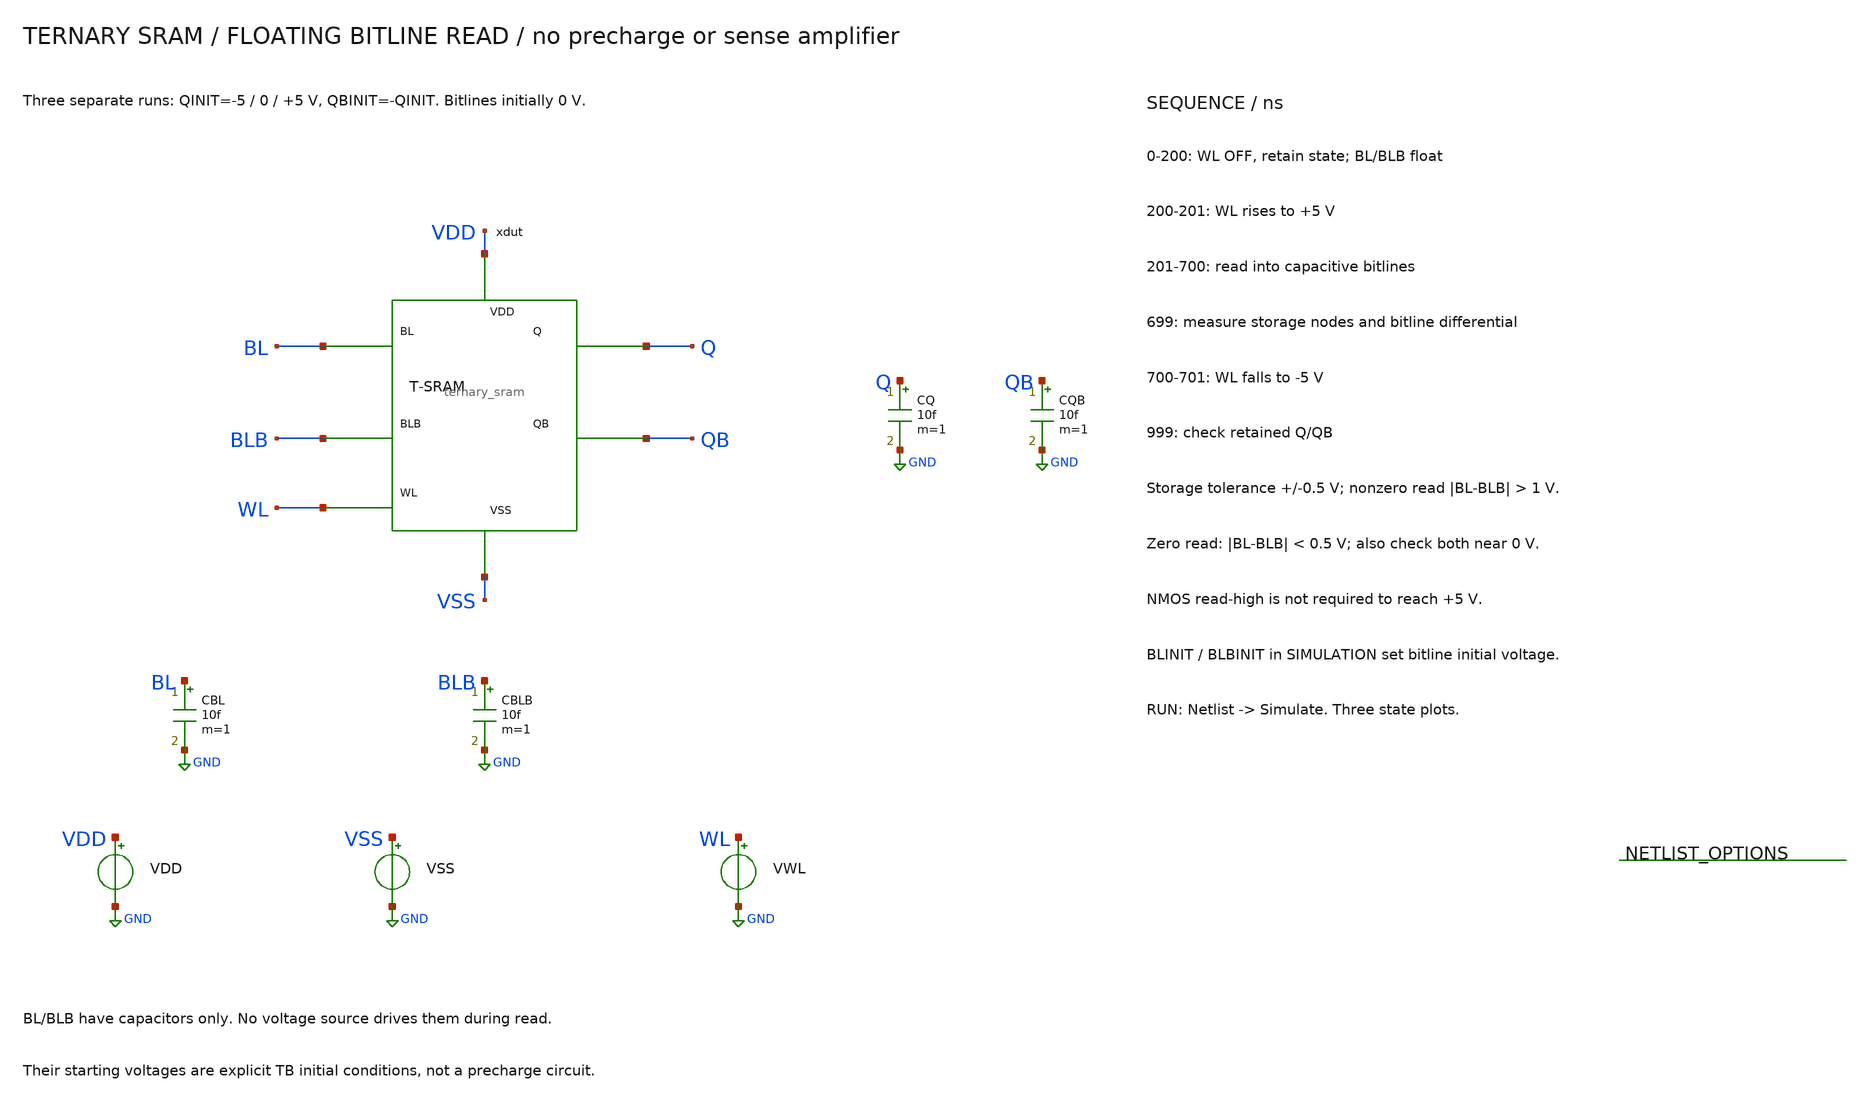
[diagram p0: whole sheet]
** sch_path: member_project/balanced-ternary-logic/PenguinEino/ternary_sram_read_tb.sch
**.subckt ternary_sram_read_tb
xdut BL BLB WL Q QB VDD VSS ternary_sram
CQ Q GND 10f m=1
CQB QB GND 10f m=1
CBL BL GND 10f m=1
CBLB BLB GND 10f m=1
VDD VDD GND 5
VSS VSS GND -5
VWL WL GND PWL(0 -5 200n -5 201n 5 700n 5 701n -5 1000n -5)
**** begin user architecture code
 .include $::LIB/ip62_models

.temp 27
.param QINIT=-5 BLINIT=0 BLBINIT=0
.ic v(Q)='QINIT' v(QB)='-QINIT' v(BL)='BLINIT' v(BLB)='BLBINIT'
.control
save all
set wr_singlescale
set wr_vecnames
setplot const
let failures=0
tran 0.2n 1000n 0 0.5n
let diff=v(BL)-v(BLB)
meas tran q0_199 find v(Q) at=199n
if abs(q0_199-(-5)) > 0.5
let const.failures=const.failures+1
echo FAIL: q0_199 expected -5 V
end
meas tran qb0_199 find v(QB) at=199n
if abs(qb0_199-(5)) > 0.5
let const.failures=const.failures+1
echo FAIL: qb0_199 expected 5 V
end
meas tran q0_699 find v(Q) at=699n
if abs(q0_699-(-5)) > 0.5
let const.failures=const.failures+1
echo FAIL: q0_699 expected -5 V
end
meas tran qb0_699 find v(QB) at=699n
if abs(qb0_699-(5)) > 0.5
let const.failures=const.failures+1
echo FAIL: qb0_699 expected 5 V
end
meas tran q0_999 find v(Q) at=999n
if abs(q0_999-(-5)) > 0.5
let const.failures=const.failures+1
echo FAIL: q0_999 expected -5 V
end
meas tran qb0_999 find v(QB) at=999n
if abs(qb0_999-(5)) > 0.5
let const.failures=const.failures+1
echo FAIL: qb0_999 expected 5 V
end
meas tran read_diff_0 find diff at=699n
meas tran read_bl_0 find v(BL) at=699n
meas tran read_blb_0 find v(BLB) at=699n
if read_diff_0 > -1
let const.failures=const.failures+1
echo FAIL: read differential state -5
end
plot v(Q) v(QB) v(BL) v(BLB) ylimit -5.5 5.5 title 'SRAM floating read: initial Q=-5 V'
wrdata ternary_sram_read_0.txt v(Q) v(QB) v(BL) v(BLB) v(WL)
alterparam QINIT=0
reset
save all
tran 0.2n 1000n 0 0.5n
let diff=v(BL)-v(BLB)
meas tran q1_199 find v(Q) at=199n
if abs(q1_199-(0)) > 0.5
let const.failures=const.failures+1
echo FAIL: q1_199 expected 0 V
end
meas tran qb1_199 find v(QB) at=199n
if abs(qb1_199-(0)) > 0.5
let const.failures=const.failures+1
echo FAIL: qb1_199 expected 0 V
end
meas tran q1_699 find v(Q) at=699n
if abs(q1_699-(0)) > 0.5
let const.failures=const.failures+1
echo FAIL: q1_699 expected 0 V
end
meas tran qb1_699 find v(QB) at=699n
if abs(qb1_699-(0)) > 0.5
let const.failures=const.failures+1
echo FAIL: qb1_699 expected 0 V
end
meas tran q1_999 find v(Q) at=999n
if abs(q1_999-(0)) > 0.5
let const.failures=const.failures+1
echo FAIL: q1_999 expected 0 V
end
meas tran qb1_999 find v(QB) at=999n
if abs(qb1_999-(0)) > 0.5
let const.failures=const.failures+1
echo FAIL: qb1_999 expected 0 V
end
meas tran read_diff_1 find diff at=699n
meas tran read_bl_1 find v(BL) at=699n
meas tran read_blb_1 find v(BLB) at=699n
if abs(read_diff_1) > 0.5
let const.failures=const.failures+1
echo FAIL: read differential state 0
end
meas tran zero_bl find v(BL) at=699n
if abs(zero_bl-(0)) > 0.5
let const.failures=const.failures+1
echo FAIL: zero_bl expected 0 V
end
meas tran zero_blb find v(BLB) at=699n
if abs(zero_blb-(0)) > 0.5
let const.failures=const.failures+1
echo FAIL: zero_blb expected 0 V
end
plot v(Q) v(QB) v(BL) v(BLB) ylimit -5.5 5.5 title 'SRAM floating read: initial Q=0 V'
wrdata ternary_sram_read_1.txt v(Q) v(QB) v(BL) v(BLB) v(WL)
alterparam QINIT=5
reset
save all
tran 0.2n 1000n 0 0.5n
let diff=v(BL)-v(BLB)
meas tran q2_199 find v(Q) at=199n
if abs(q2_199-(5)) > 0.5
let const.failures=const.failures+1
echo FAIL: q2_199 expected 5 V
end
meas tran qb2_199 find v(QB) at=199n
if abs(qb2_199-(-5)) > 0.5
let const.failures=const.failures+1
echo FAIL: qb2_199 expected -5 V
end
meas tran q2_699 find v(Q) at=699n
if abs(q2_699-(5)) > 0.5
let const.failures=const.failures+1
echo FAIL: q2_699 expected 5 V
end
meas tran qb2_699 find v(QB) at=699n
if abs(qb2_699-(-5)) > 0.5
let const.failures=const.failures+1
echo FAIL: qb2_699 expected -5 V
end
meas tran q2_999 find v(Q) at=999n
if abs(q2_999-(5)) > 0.5
let const.failures=const.failures+1
echo FAIL: q2_999 expected 5 V
end
meas tran qb2_999 find v(QB) at=999n
if abs(qb2_999-(-5)) > 0.5
let const.failures=const.failures+1
echo FAIL: qb2_999 expected -5 V
end
meas tran read_diff_2 find diff at=699n
meas tran read_bl_2 find v(BL) at=699n
meas tran read_blb_2 find v(BLB) at=699n
if read_diff_2 < 1
let const.failures=const.failures+1
echo FAIL: read differential state 5
end
plot v(Q) v(QB) v(BL) v(BLB) ylimit -5.5 5.5 title 'SRAM floating read: initial Q=5 V'
wrdata ternary_sram_read_2.txt v(Q) v(QB) v(BL) v(BLB) v(WL)
if const.failures = 0
echo PASS: three-state floating-bitline read and retention
else
echo FAIL: three-state floating-bitline read and retention
end
print const.failures
.endc

**** end user architecture code
**.ends

* expanding   symbol:  /home/ishi-kai/balanced-ternary-logic/ternary_sram.sym # of pins=7
** sym_path: member_project/balanced-ternary-logic/PenguinEino/ternary_sram.sym
** sch_path: member_project/balanced-ternary-logic/PenguinEino/ternary_sram.sch
.subckt ternary_sram BL BLB WL Q QB VDD VSS
*.ipin WL
*.iopin BL
*.iopin BLB
*.opin Q
*.opin QB
*.iopin VDD
*.iopin VSS
x_store Q QB VDD VSS ternary_latch
XXM_A Q WL BL VSS NMOS w=3.4u l=1u nrd=0 nrs=0 m=1
XXM_AB QB WL BLB VSS NMOS w=3.4u l=1u nrd=0 nrs=0 m=1
.ends


* expanding   symbol:  /home/ishi-kai/balanced-ternary-logic/ternary_latch.sym # of pins=4
** sym_path: member_project/balanced-ternary-logic/PenguinEino/ternary_latch.sym
** sch_path: member_project/balanced-ternary-logic/PenguinEino/ternary_latch.sch
.subckt ternary_latch Q QB VDD VSS
*.opin Q
*.opin QB
*.iopin VDD
*.iopin VSS
x_q QB Q VDD VSS inverter
x_qb Q QB VDD VSS inverter
.ends


* expanding   symbol:  /home/ishi-kai/balanced-ternary-logic/inverter.sym # of pins=4
** sym_path: member_project/balanced-ternary-logic/PenguinEino/inverter.sym
** sch_path: member_project/balanced-ternary-logic/PenguinEino/inverter.sch
.subckt inverter vin vout VDD VSS
*.iopin VDD
*.ipin vin
*.opin vout
*.iopin VSS
XXM1 net1 vin VDD VDD PMOS w=13.5u l=1u nrd=0 nrs=0 m=1
XR1 net1 vout VDD F_RR w=2.8e-06 l=30e-06 R=1 tc1=0 tc2=0 m=1
XR2 vout net2 VDD F_RR w=2.8e-06 l=30e-06 R=1 tc1=0 tc2=0 m=1
XXM2 net2 vin VSS VSS NMOS w=5u l=1u nrd=0 nrs=0 m=1
.ends

.GLOBAL GND
.end
